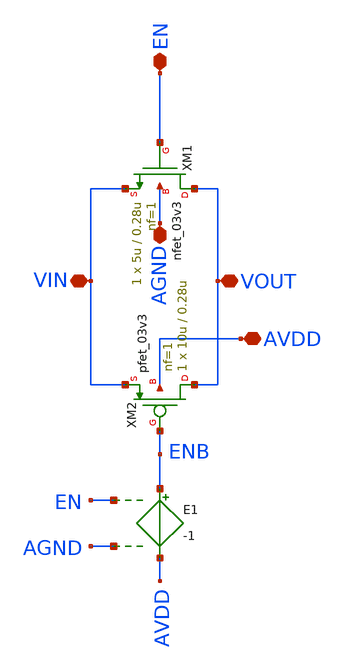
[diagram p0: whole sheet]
** sch_path: tg.sch
**.subckt tg AGND AVDD EN VOUT VIN
*.iopin AGND
*.iopin AVDD
*.iopin EN
*.iopin VOUT
*.iopin VIN
XM1 VOUT EN VIN AGND nfet_03v3 L=0.28u W=5u nf=1 ad='int((nf+1)/2) * W/nf * 0.18u' as='int((nf+2)/2) * W/nf * 0.18u'
+ pd='2*int((nf+1)/2) * (W/nf + 0.18u)' ps='2*int((nf+2)/2) * (W/nf + 0.18u)' nrd='0.18u / W' nrs='0.18u / W'
+ sa=0 sb=0 sd=0 m=1
XM2 VOUT ENB VIN AVDD pfet_03v3 L=0.28u W=10u nf=1 ad='int((nf+1)/2) * W/nf * 0.18u' as='int((nf+2)/2) * W/nf * 0.18u'
+ pd='2*int((nf+1)/2) * (W/nf + 0.18u)' ps='2*int((nf+2)/2) * (W/nf + 0.18u)' nrd='0.18u / W' nrs='0.18u / W'
+ sa=0 sb=0 sd=0 m=1
E1 ENB AVDD EN AGND -1
**.ends
.end
